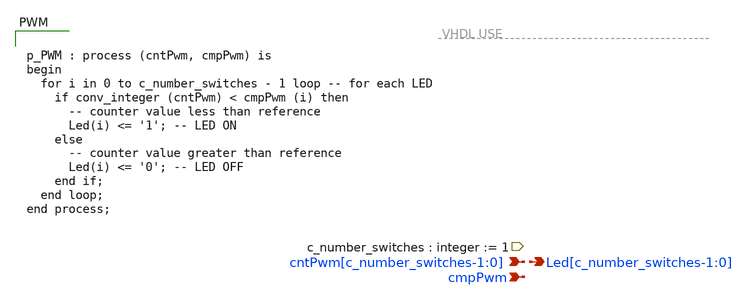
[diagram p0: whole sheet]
** sch_path: xschem/PWM.sch
**.subckt PWM cntPwm[c_number_switches-1:0] cmpPwm Led[c_number_switches-1:0]
*.ipin cntPwm[c_number_switches-1:0]
*.ipin cmpPwm
*.opin Led[c_number_switches-1:0]
**** begin user architecture code


p_PWM : process (cntPwm, cmpPwm) is
begin
  for i in 0 to c_number_switches - 1 loop -- for each LED
    if conv_integer (cntPwm) < cmpPwm (i) then
      -- counter value less than reference
      Led(i) <= '1'; -- LED ON
    else
      -- counter value greater than reference
      Led(i) <= '0'; -- LED OFF
    end if;
  end loop;
end process;


**** end user architecture code
**.ends
.end
